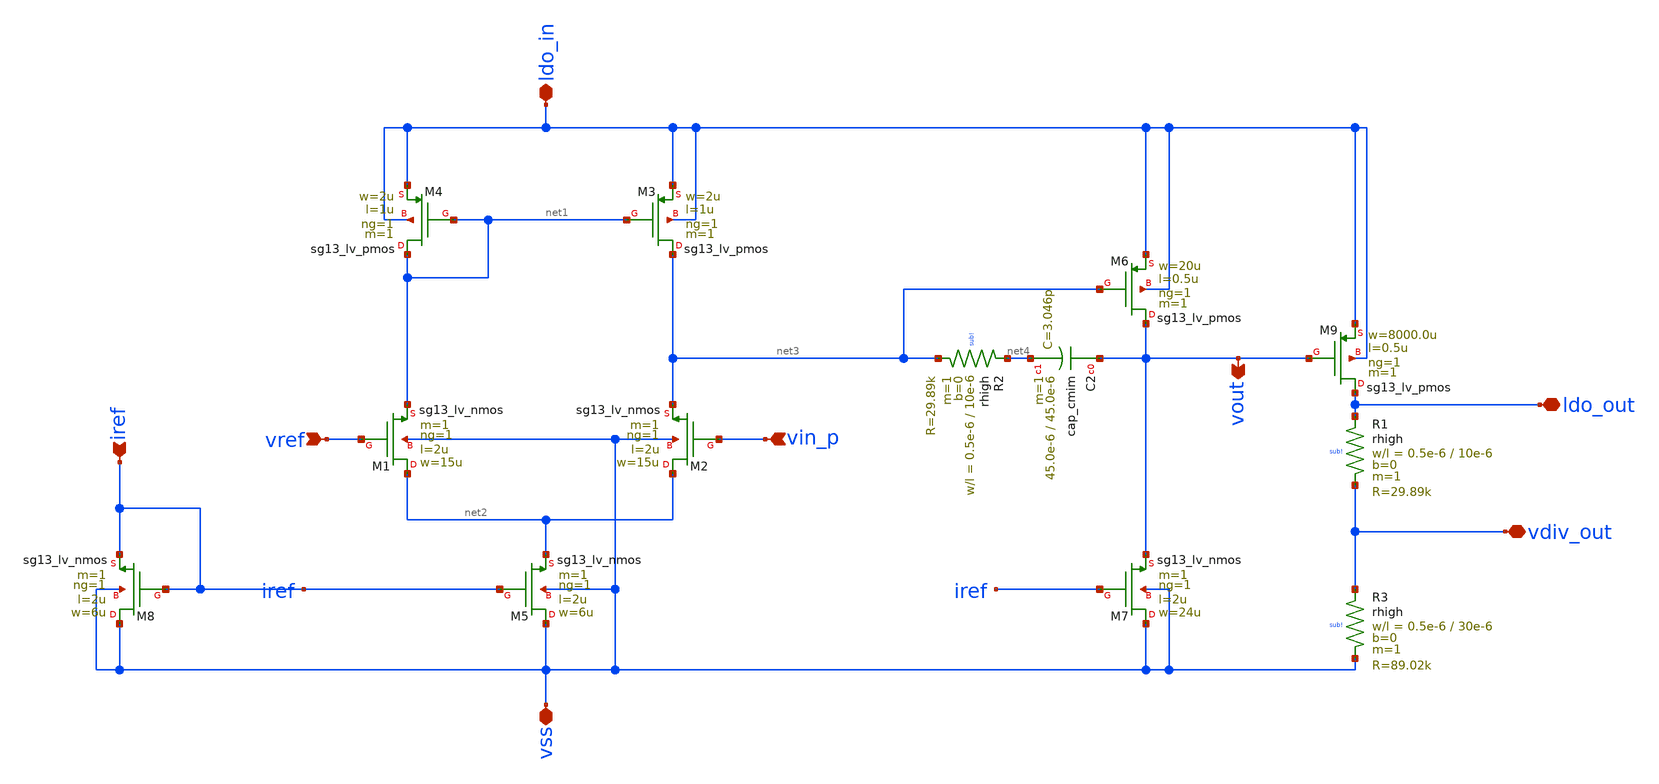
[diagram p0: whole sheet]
** sch_path: AC3E-IHP_ALDO/design_data/klayout/netlist/LDO_openloop.sch
**.subckt LDO_openloop iref vref vin_p ldo_in vss vout vdiv_out ldo_out
*.ipin iref
*.ipin vref
*.ipin vin_p
*.iopin ldo_in
*.iopin vss
*.opin vout
*.iopin vdiv_out
*.iopin ldo_out
XM1 net2 vref net1 vss sg13_lv_nmos w=15u l=2u ng=1 m=1 mm_ok=1
XM2 net2 vin_p net3 vss sg13_lv_nmos w=15u l=2u ng=1 m=1 mm_ok=1
XM3 net3 net1 ldo_in ldo_in sg13_lv_pmos w=2u l=1u ng=1 m=1 mm_ok=1
XM4 net1 net1 ldo_in ldo_in sg13_lv_pmos w=2u l=1u ng=1 m=1 mm_ok=1
XM5 vss iref net2 vss sg13_lv_nmos w=6u l=2u ng=1 m=1 mm_ok=1
XM8 vss iref iref vss sg13_lv_nmos w=6u l=2u ng=1 m=1 mm_ok=1
XM6 vout net3 ldo_in ldo_in sg13_lv_pmos w=20u l=0.5u ng=1 m=1 mm_ok=1
XM7 vss iref vout vss sg13_lv_nmos w=24u l=2u ng=1 m=1 mm_ok=1
XC2 vout net4 cap_cmim w=45.0e-6 l=45.0e-6 m=1 mm_ok=1
XR2 net4 net3 sub! rhigh w=0.5e-6 l=10e-6 m=1 b=0 mm_ok=1
XM9 ldo_out vout ldo_in ldo_in sg13_lv_pmos w=8000.0u l=0.5u ng=1 m=1 mm_ok=1
XR1 ldo_out vdiv_out sub! rhigh w=0.5e-6 l=10e-6 m=1 b=0 mm_ok=1
XR3 vdiv_out vss sub! rhigh w=0.5e-6 l=30e-6 m=1 b=0 mm_ok=1
**.ends
.end
